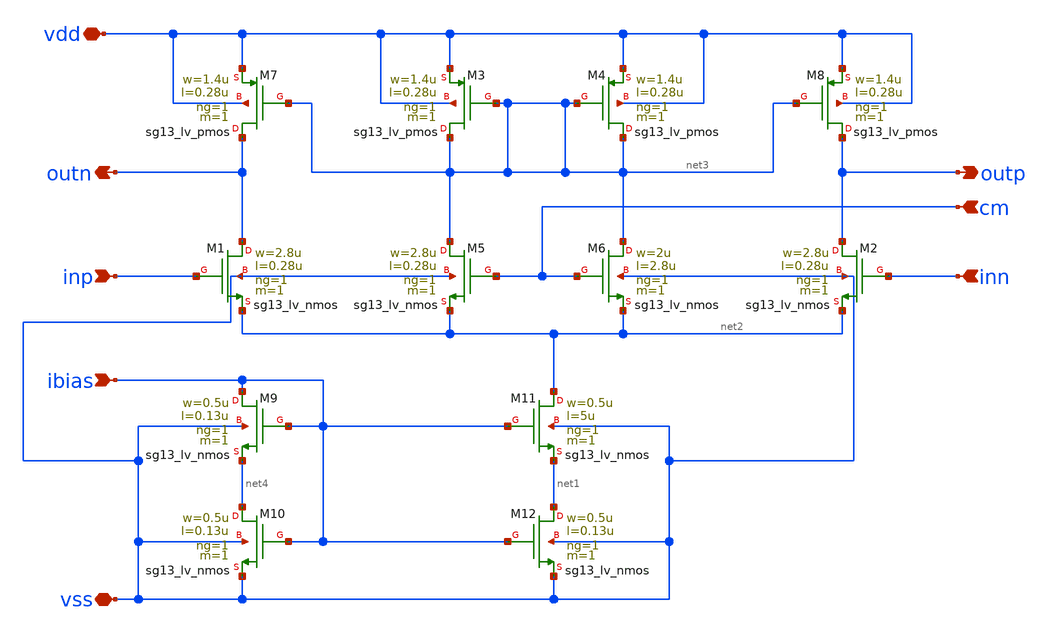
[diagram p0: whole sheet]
** sch_path: 3_Real_Cir/ota_gm_100u.sch
**.subckt ota_gm_100u inp inn outp outn vdd ibias cm vss
*.ipin inp
*.ipin inn
*.opin outp
*.opin outn
*.iopin vdd
*.ipin ibias
*.ipin cm
*.iopin vss
XM3 net3 net3 vdd vdd sg13_lv_pmos w=1.4u l=0.28u ng=1 m=1 mm_ok=1
XM4 net3 net3 vdd vdd sg13_lv_pmos w=1.4u l=0.28u ng=1 m=1 mm_ok=1
XM1 outn inp net2 vss sg13_lv_nmos w=2.8u l=0.28u ng=1 m=1 mm_ok=1
XM2 outp inn net2 vss sg13_lv_nmos w=2.8u l=0.28u ng=1 m=1 mm_ok=1
XM11 net2 ibias net1 vss sg13_lv_nmos w=0.5u l=5u ng=1 m=1 mm_ok=1
XM8 outp net3 vdd vdd sg13_lv_pmos w=1.4u l=0.28u ng=1 m=1 mm_ok=1
XM7 outn net3 vdd vdd sg13_lv_pmos w=1.4u l=0.28u ng=1 m=1 mm_ok=1
XM5 net3 cm net2 vss sg13_lv_nmos w=2.8u l=0.28u ng=1 m=1 mm_ok=1
XM6 net3 cm net2 vss sg13_lv_nmos w=2u l=2.8u ng=1 m=1 mm_ok=1
XM12 net1 ibias vss vss sg13_lv_nmos w=0.5u l=0.13u ng=1 m=1 mm_ok=1
XM9 ibias ibias net4 vss sg13_lv_nmos w=0.5u l=0.13u ng=1 m=1 mm_ok=1
XM10 net4 ibias vss vss sg13_lv_nmos w=0.5u l=0.13u ng=1 m=1 mm_ok=1
**.ends
.end
